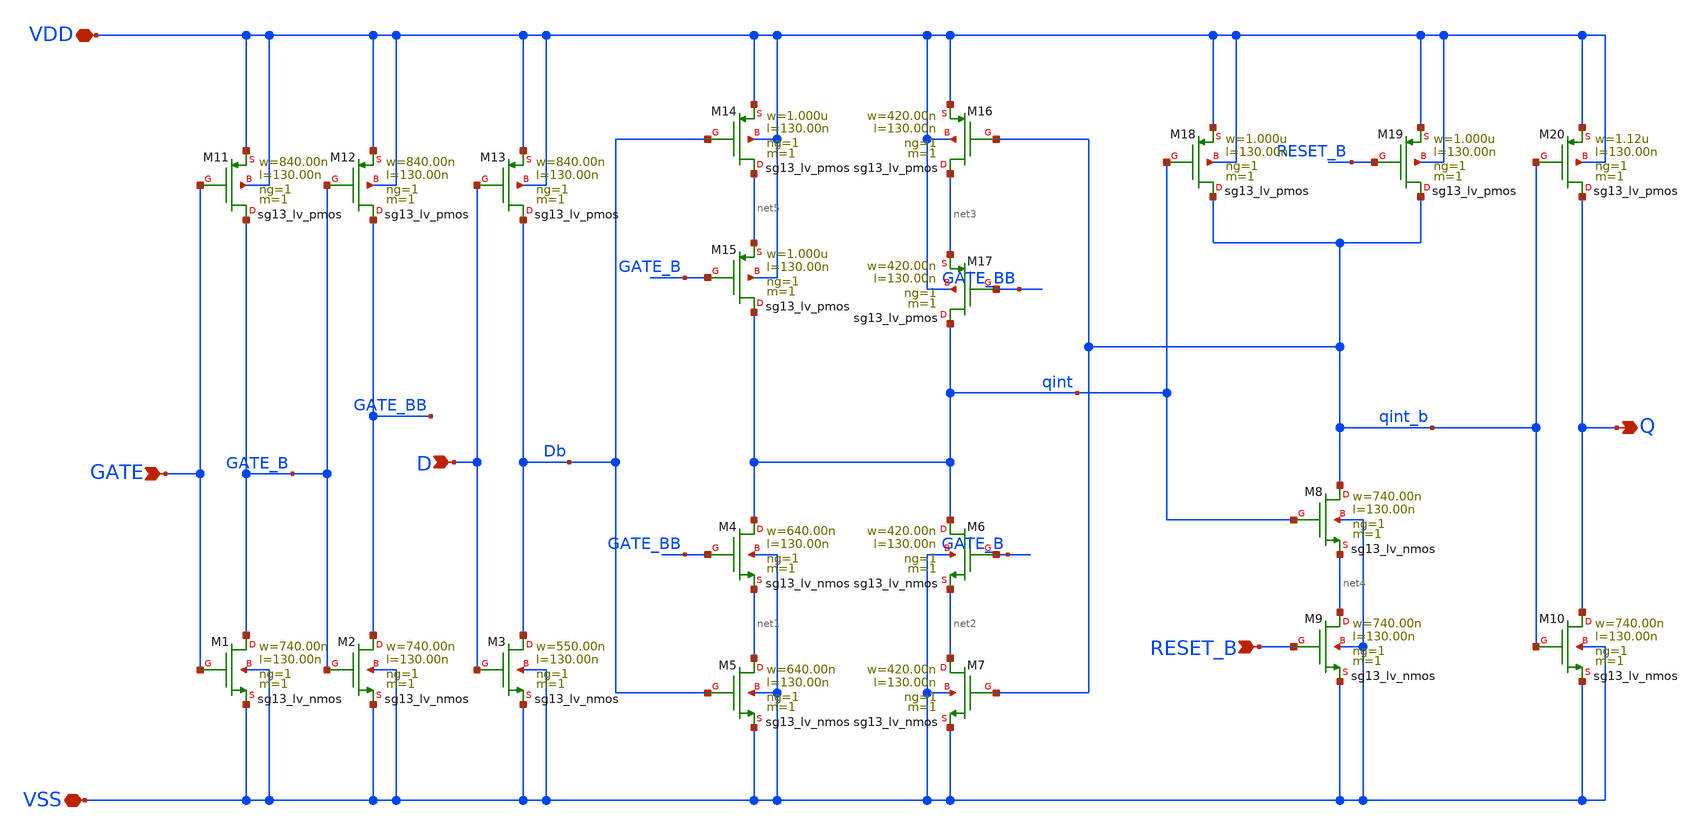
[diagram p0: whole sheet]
** sch_path: ihp-sg13g2/libs.tech/xschem/sg13g2_stdcells/sg13g2_dlhrq_1.sch
* Copyright 2023 IHP PDK Authors
* Licensed under the Apache License, Version 2.0 (the "License");
* you may not use this file except in compliance with the License.
* You may obtain a copy of the License at
* https://www.apache.org/licenses/LICENSE-2.0
* Unless required by applicable law or agreed to in writing, software
* distributed under the License is distributed on an "AS IS" BASIS,
* WITHOUT WARRANTIES OR CONDITIONS OF ANY KIND, either express or implied.
* See the License for the specific language governing permissions and
* limitations under the License.
**.subckt sg13g2_dlhrq_1 D GATE RESET_B Q VDD VSS
*.ipin D
*.ipin GATE
*.ipin RESET_B
*.opin Q
*.iopin VDD
*.iopin VSS
XM1 GATE_B GATE VSS VSS sg13_lv_nmos w=740.00n l=130.00n ng=1 m=1 mm_ok=1
XM2 GATE_BB GATE_B VSS VSS sg13_lv_nmos w=740.00n l=130.00n ng=1 m=1 mm_ok=1
XM3 Db D VSS VSS sg13_lv_nmos w=550.00n l=130.00n ng=1 m=1 mm_ok=1
XM4 qint GATE_BB net1 VSS sg13_lv_nmos w=640.00n l=130.00n ng=1 m=1 mm_ok=1
XM5 net1 Db VSS VSS sg13_lv_nmos w=640.00n l=130.00n ng=1 m=1 mm_ok=1
XM6 qint GATE_B net2 VSS sg13_lv_nmos w=420.00n l=130.00n ng=1 m=1 mm_ok=1
XM7 net2 qint_b VSS VSS sg13_lv_nmos w=420.00n l=130.00n ng=1 m=1 mm_ok=1
XM8 qint_b qint net4 VSS sg13_lv_nmos w=740.00n l=130.00n ng=1 m=1 mm_ok=1
XM9 net4 RESET_B VSS VSS sg13_lv_nmos w=740.00n l=130.00n ng=1 m=1 mm_ok=1
XM10 Q qint_b VSS VSS sg13_lv_nmos w=740.00n l=130.00n ng=1 m=1 mm_ok=1
XM11 GATE_B GATE VDD VDD sg13_lv_pmos w=840.00n l=130.00n ng=1 m=1 mm_ok=1
XM12 GATE_BB GATE_B VDD VDD sg13_lv_pmos w=840.00n l=130.00n ng=1 m=1 mm_ok=1
XM13 Db D VDD VDD sg13_lv_pmos w=840.00n l=130.00n ng=1 m=1 mm_ok=1
XM14 net5 Db VDD VDD sg13_lv_pmos w=1.000u l=130.00n ng=1 m=1 mm_ok=1
XM15 qint GATE_B net5 VDD sg13_lv_pmos w=1.000u l=130.00n ng=1 m=1 mm_ok=1
XM16 net3 qint_b VDD VDD sg13_lv_pmos w=420.00n l=130.00n ng=1 m=1 mm_ok=1
XM17 qint GATE_BB net3 VDD sg13_lv_pmos w=420.00n l=130.00n ng=1 m=1 mm_ok=1
XM18 qint_b qint VDD VDD sg13_lv_pmos w=1.000u l=130.00n ng=1 m=1 mm_ok=1
XM19 qint_b RESET_B VDD VDD sg13_lv_pmos w=1.000u l=130.00n ng=1 m=1 mm_ok=1
XM20 Q qint_b VDD VDD sg13_lv_pmos w=1.12u l=130.00n ng=1 m=1 mm_ok=1
**.ends
.end
